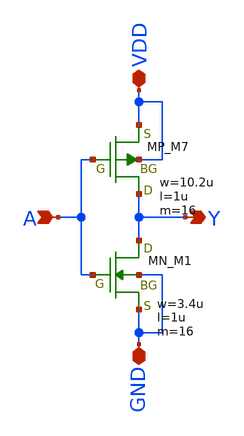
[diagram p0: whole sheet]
** sch_path: libs.tech/xschem/TR-1um_5_stdcell/INV_X16.sch
**.subckt INV_X16 A Y GND VDD
*.ipin A
*.opin Y
*.iopin GND
*.iopin VDD
XM7 Y A VDD VDD PMOS w=10.2u l=1u nrd=0 nrs=0 m=16
XM1 Y A GND GND NMOS w=3.4u l=1u nrd=0 nrs=0 m=16
**.ends
.end
